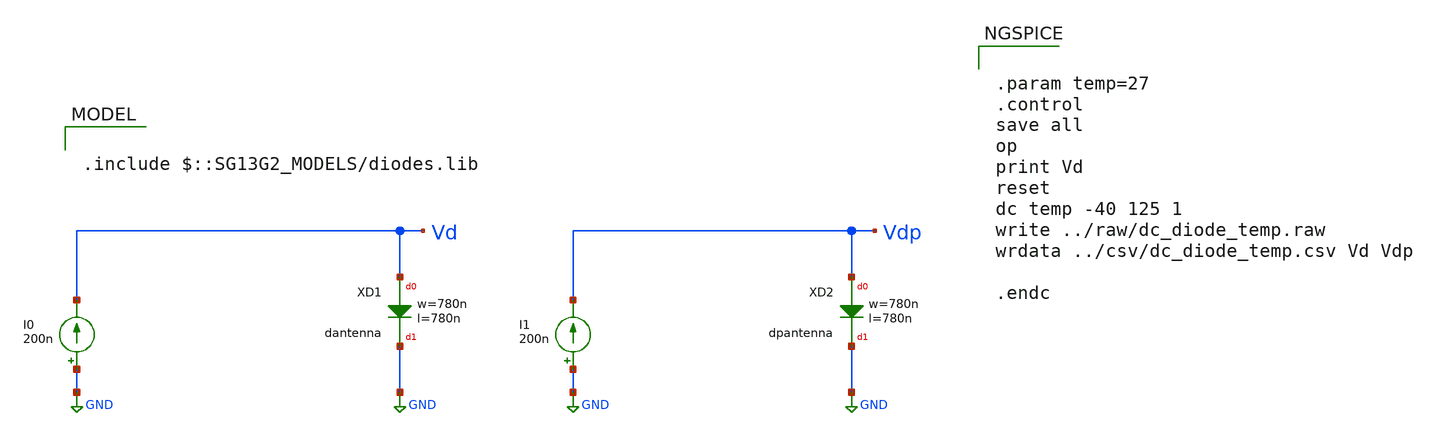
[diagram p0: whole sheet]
** sch_path: ihp-sg13g2/libs.tech/xschem/sg13g2_tests/dc_diode_temp.sch
* Copyright 2023 IHP PDK Authors
**.subckt dc_diode_temp
XD1 Vd GND dantenna l=780n w=780n
I0 GND Vd 200n
I1 GND Vdp 200n
XXD2 Vdp GND dpantenna l=780n w=780n
**** begin user architecture code

.include $::SG13G2_MODELS/diodes.lib



.param temp=27
.control
save all
op
print Vd
reset
dc temp -40 125 1
write ../raw/dc_diode_temp.raw
wrdata ../csv/dc_diode_temp.csv Vd Vdp

.endc


**** end user architecture code
**.ends
.GLOBAL GND
.end
